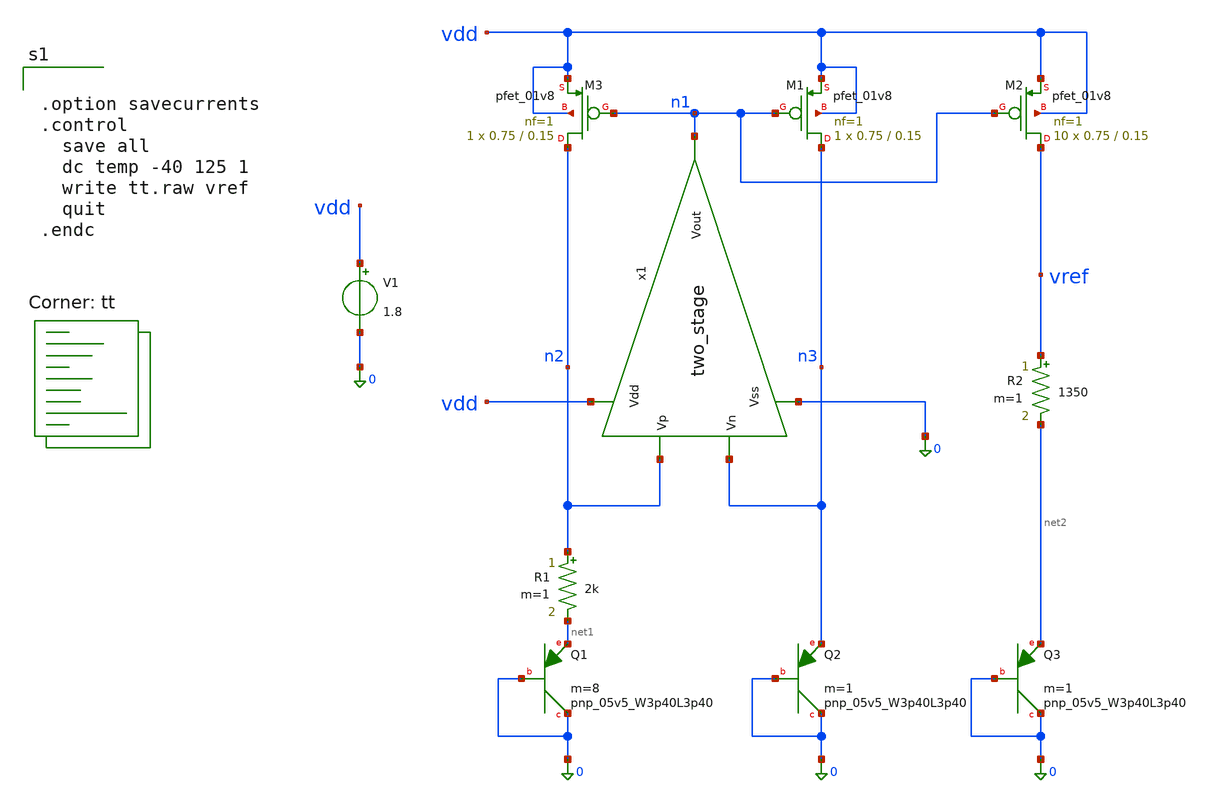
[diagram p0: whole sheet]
** sch_path: Bandgap/Bandgap.sch
**.subckt Bandgap
R1 n2 net1 2k m=1
V1 vdd 0 1.8
XM1 n3 n1 vdd vdd sky130_fd_pr__pfet_01v8 L=0.15 W=0.75 nf=1 ad='int((1 + 1)/2) * 0.75 / 1 * 0.29' as='int((1 + 2)/2) * 0.75 / 1 * 0.29'
+ pd='2*int((1 + 1)/2) * (0.75 / 1 + 0.29)' ps='2*int((1 + 2)/2) * (0.75 / 1 + 0.29)' nrd='0.29 / 0.75 '
+ nrs='0.29 / 0.75 ' sa=0 sb=0 sd=0 mult=1 m=1
XM3 n2 n1 vdd vdd sky130_fd_pr__pfet_01v8 L=0.15 W=0.75 nf=1 ad='int((1 + 1)/2) * 0.75 / 1 * 0.29' as='int((1 + 2)/2) * 0.75 / 1 * 0.29'
+ pd='2*int((1 + 1)/2) * (0.75 / 1 + 0.29)' ps='2*int((1 + 2)/2) * (0.75 / 1 + 0.29)' nrd='0.29 / 0.75 '
+ nrs='0.29 / 0.75 ' sa=0 sb=0 sd=0 mult=1 m=1
XQ1 0 0 net1 sky130_fd_pr__pnp_05v5_W3p40L3p40 m=8
XQ2 0 0 n3 sky130_fd_pr__pnp_05v5_W3p40L3p40 m=1
x1 vdd n1 n2 n3 0 two_stage
XM2 vref n1 vdd vdd sky130_fd_pr__pfet_01v8 L=0.15 W=0.75 nf=1 ad='int((1 + 1)/2) * 0.75 / 1 * 0.29'
+ as='int((1 + 2)/2) * 0.75 / 1 * 0.29' pd='2*int((1 + 1)/2) * (0.75 / 1 + 0.29)' ps='2*int((1 + 2)/2) * (0.75 / 1 + 0.29)'
+ nrd='0.29 / 0.75 ' nrs='0.29 / 0.75 ' sa=0 sb=0 sd=0 mult=10 m=10
R2 vref net2 1350 m=1
XQ3 0 0 net2 sky130_fd_pr__pnp_05v5_W3p40L3p40 m=1
**** begin user architecture code


.option savecurrents
.control
  save all
  dc temp -40 125 1
  write tt.raw vref
  quit
.endc


.lib $::SKYWATER_MODELS/sky130.lib.spice tt
**** end user architecture code
**.ends

* expanding   symbol:  two_stage.sym # of pins=5
** sym_path: Bandgap/No_Ideal/two_stage.sym
** sch_path: Bandgap/No_Ideal/two_stage.sch
.subckt two_stage Vdd Vout Vp Vn Vss
*.ipin Vdd
*.opin Vout
*.ipin Vss
*.ipin Vp
*.ipin Vn
XM1 net1 net1 Vdd Vdd sky130_fd_pr__pfet_01v8 L=0.30 W=7.2 nf=1 ad='int((1 + 1)/2) * 7.2 / 1 * 0.29'
+ as='int((1 + 2)/2) * 7.2 / 1 * 0.29' pd='2*int((1 + 1)/2) * (7.2 / 1 + 0.29)' ps='2*int((1 + 2)/2) * (7.2 / 1 + 0.29)'
+ nrd='0.29 / 7.2 ' nrs='0.29 / 7.2 ' sa=0 sb=0 sd=0 mult=1 m=1
XM2 net1 Vp net3 net3 sky130_fd_pr__nfet_01v8 L=0.15 W=0.66 nf=1 ad='int((1 + 1)/2) * 0.66 / 1 * 0.29'
+ as='int((1 + 2)/2) * 0.66 / 1 * 0.29' pd='2*int((1 + 1)/2) * (0.66 / 1 + 0.29)' ps='2*int((1 + 2)/2) * (0.66 / 1 + 0.29)'
+ nrd='0.29 / 0.66 ' nrs='0.29 / 0.66 ' sa=0 sb=0 sd=0 mult=1 m=1
XM3 net2 net1 Vdd Vdd sky130_fd_pr__pfet_01v8 L=0.30 W=7.2 nf=1 ad='int((1 + 1)/2) * 7.2 / 1 * 0.29'
+ as='int((1 + 2)/2) * 7.2 / 1 * 0.29' pd='2*int((1 + 1)/2) * (7.2 / 1 + 0.29)' ps='2*int((1 + 2)/2) * (7.2 / 1 + 0.29)'
+ nrd='0.29 / 7.2 ' nrs='0.29 / 7.2 ' sa=0 sb=0 sd=0 mult=1 m=1
XM4 net2 Vn net3 net3 sky130_fd_pr__nfet_01v8 L=0.15 W=0.66 nf=1 ad='int((1 + 1)/2) * 0.66 / 1 * 0.29'
+ as='int((1 + 2)/2) * 0.66 / 1 * 0.29' pd='2*int((1 + 1)/2) * (0.66 / 1 + 0.29)' ps='2*int((1 + 2)/2) * (0.66 / 1 + 0.29)'
+ nrd='0.29 / 0.66 ' nrs='0.29 / 0.66 ' sa=0 sb=0 sd=0 mult=1 m=1
XM5 Vout net2 Vdd Vdd sky130_fd_pr__pfet_01v8 L=0.30 W=30 nf=1 ad='int((1 + 1)/2) * 30 / 1 * 0.29' as='int((1 + 2)/2) * 30 / 1 * 0.29'
+ pd='2*int((1 + 1)/2) * (30 / 1 + 0.29)' ps='2*int((1 + 2)/2) * (30 / 1 + 0.29)' nrd='0.29 / 30 ' nrs='0.29 / 30 '
+ sa=0 sb=0 sd=0 mult=2 m=2
C1 Vout net4 2p m=1
R1 net4 net2 9k m=1
C2 Vss Vout 5p m=1
R2 net5 net6 26k m=1
R3 net6 Vdd 54k m=1
XM6 net5 net6 Vss Vss sky130_fd_pr__nfet_01v8 L=0.50 W=5 nf=1 ad='int((1 + 1)/2) * 5 / 1 * 0.29' as='int((1 + 2)/2) * 5 / 1 * 0.29'
+ pd='2*int((1 + 1)/2) * (5 / 1 + 0.29)' ps='2*int((1 + 2)/2) * (5 / 1 + 0.29)' nrd='0.29 / 5 ' nrs='0.29 / 5 '
+ sa=0 sb=0 sd=0 mult=1 m=1
XM7 net3 net6 Vss Vss sky130_fd_pr__nfet_01v8 L=0.50 W=5 nf=1 ad='int((1 + 1)/2) * 5 / 1 * 0.29' as='int((1 + 2)/2) * 5 / 1 * 0.29'
+ pd='2*int((1 + 1)/2) * (5 / 1 + 0.29)' ps='2*int((1 + 2)/2) * (5 / 1 + 0.29)' nrd='0.29 / 5 ' nrs='0.29 / 5 '
+ sa=0 sb=0 sd=0 mult=1 m=1
XM8 net7 net7 Vss Vss sky130_fd_pr__nfet_01v8 L=0.50 W=5 nf=1 ad='int((1 + 1)/2) * 5 / 1 * 0.29' as='int((1 + 2)/2) * 5 / 1 * 0.29'
+ pd='2*int((1 + 1)/2) * (5 / 1 + 0.29)' ps='2*int((1 + 2)/2) * (5 / 1 + 0.29)' nrd='0.29 / 5 ' nrs='0.29 / 5 '
+ sa=0 sb=0 sd=0 mult=1 m=1
XM9 Vout net7 Vss Vss sky130_fd_pr__nfet_01v8 L=0.50 W=5 nf=1 ad='int((1 + 1)/2) * 5 / 1 * 0.29' as='int((1 + 2)/2) * 5 / 1 * 0.29'
+ pd='2*int((1 + 1)/2) * (5 / 1 + 0.29)' ps='2*int((1 + 2)/2) * (5 / 1 + 0.29)' nrd='0.29 / 5 ' nrs='0.29 / 5 '
+ sa=0 sb=0 sd=0 mult=1 m=1
I0 Vdd net7 75u
.ends

.end
